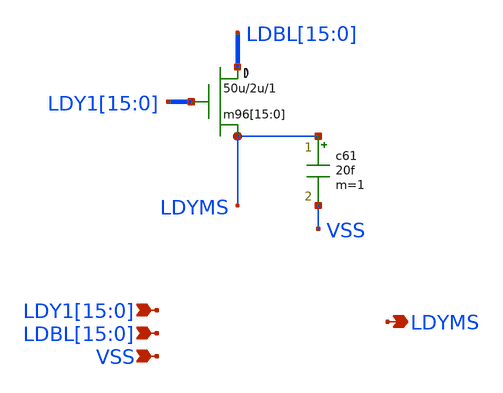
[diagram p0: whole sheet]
** sch_path: xschem_libs_newsym/rom8k/rom2_coldec/schematic/rom2_coldec.sch
* Copyright (C) 1998-2024 Stefan Frederik Schippers
* This program is free software; you can redistribute it and/or modify
* it under the terms of the GNU General Public License as published by
* the Free Software Foundation; either version 2 of the License, or
* (at your option) any later version.
* This program is distributed in the hope that it will be useful,
* but WITHOUT ANY WARRANTY; without even the implied warranty of
* MERCHANTABILITY or FITNESS FOR A PARTICULAR PURPOSE.  See the
* GNU General Public License for more details.
* You should have received a copy of the GNU General Public License
* along with this program; if not, write to the Free Software
**.subckt rom2_coldec LDYMS
*+ LDY1[15],LDY1[14],LDY1[13],LDY1[12],LDY1[11],LDY1[10],LDY1[9],LDY1[8],LDY1[7],LDY1[6],LDY1[5],LDY1[4],LDY1[3],LDY1[2],LDY1[1],LDY1[0]
*+ LDBL[15],LDBL[14],LDBL[13],LDBL[12],LDBL[11],LDBL[10],LDBL[9],LDBL[8],LDBL[7],LDBL[6],LDBL[5],LDBL[4],LDBL[3],LDBL[2],LDBL[1],LDBL[0] VSS
*.opin LDYMS
*.ipin
*+ LDY1[15],LDY1[14],LDY1[13],LDY1[12],LDY1[11],LDY1[10],LDY1[9],LDY1[8],LDY1[7],LDY1[6],LDY1[5],LDY1[4],LDY1[3],LDY1[2],LDY1[1],LDY1[0]
*.ipin
*+ LDBL[15],LDBL[14],LDBL[13],LDBL[12],LDBL[11],LDBL[10],LDBL[9],LDBL[8],LDBL[7],LDBL[6],LDBL[5],LDBL[4],LDBL[3],LDBL[2],LDBL[1],LDBL[0]
*.ipin VSS
m96[15] LDBL[15] LDY1[15] LDYMS 0 cmosn w=50u l=2u ad={50u *4.4u} as={50u *4.4u} pd={50u *2 + 8.8u} ps={50u *2 + 8.8u}
+ m=1
m96[14] LDBL[14] LDY1[14] LDYMS 0 cmosn w=50u l=2u ad={50u *4.4u} as={50u *4.4u} pd={50u *2 + 8.8u} ps={50u *2 + 8.8u}
+ m=1
m96[13] LDBL[13] LDY1[13] LDYMS 0 cmosn w=50u l=2u ad={50u *4.4u} as={50u *4.4u} pd={50u *2 + 8.8u} ps={50u *2 + 8.8u}
+ m=1
m96[12] LDBL[12] LDY1[12] LDYMS 0 cmosn w=50u l=2u ad={50u *4.4u} as={50u *4.4u} pd={50u *2 + 8.8u} ps={50u *2 + 8.8u}
+ m=1
m96[11] LDBL[11] LDY1[11] LDYMS 0 cmosn w=50u l=2u ad={50u *4.4u} as={50u *4.4u} pd={50u *2 + 8.8u} ps={50u *2 + 8.8u}
+ m=1
m96[10] LDBL[10] LDY1[10] LDYMS 0 cmosn w=50u l=2u ad={50u *4.4u} as={50u *4.4u} pd={50u *2 + 8.8u} ps={50u *2 + 8.8u}
+ m=1
m96[9] LDBL[9] LDY1[9] LDYMS 0 cmosn w=50u l=2u ad={50u *4.4u} as={50u *4.4u} pd={50u *2 + 8.8u} ps={50u *2 + 8.8u}
+ m=1
m96[8] LDBL[8] LDY1[8] LDYMS 0 cmosn w=50u l=2u ad={50u *4.4u} as={50u *4.4u} pd={50u *2 + 8.8u} ps={50u *2 + 8.8u}
+ m=1
m96[7] LDBL[7] LDY1[7] LDYMS 0 cmosn w=50u l=2u ad={50u *4.4u} as={50u *4.4u} pd={50u *2 + 8.8u} ps={50u *2 + 8.8u}
+ m=1
m96[6] LDBL[6] LDY1[6] LDYMS 0 cmosn w=50u l=2u ad={50u *4.4u} as={50u *4.4u} pd={50u *2 + 8.8u} ps={50u *2 + 8.8u}
+ m=1
m96[5] LDBL[5] LDY1[5] LDYMS 0 cmosn w=50u l=2u ad={50u *4.4u} as={50u *4.4u} pd={50u *2 + 8.8u} ps={50u *2 + 8.8u}
+ m=1
m96[4] LDBL[4] LDY1[4] LDYMS 0 cmosn w=50u l=2u ad={50u *4.4u} as={50u *4.4u} pd={50u *2 + 8.8u} ps={50u *2 + 8.8u}
+ m=1
m96[3] LDBL[3] LDY1[3] LDYMS 0 cmosn w=50u l=2u ad={50u *4.4u} as={50u *4.4u} pd={50u *2 + 8.8u} ps={50u *2 + 8.8u}
+ m=1
m96[2] LDBL[2] LDY1[2] LDYMS 0 cmosn w=50u l=2u ad={50u *4.4u} as={50u *4.4u} pd={50u *2 + 8.8u} ps={50u *2 + 8.8u}
+ m=1
m96[1] LDBL[1] LDY1[1] LDYMS 0 cmosn w=50u l=2u ad={50u *4.4u} as={50u *4.4u} pd={50u *2 + 8.8u} ps={50u *2 + 8.8u}
+ m=1
m96[0] LDBL[0] LDY1[0] LDYMS 0 cmosn w=50u l=2u ad={50u *4.4u} as={50u *4.4u} pd={50u *2 + 8.8u} ps={50u *2 + 8.8u}
+ m=1
c61 LDYMS VSS 20f m=1
**.ends
.end
